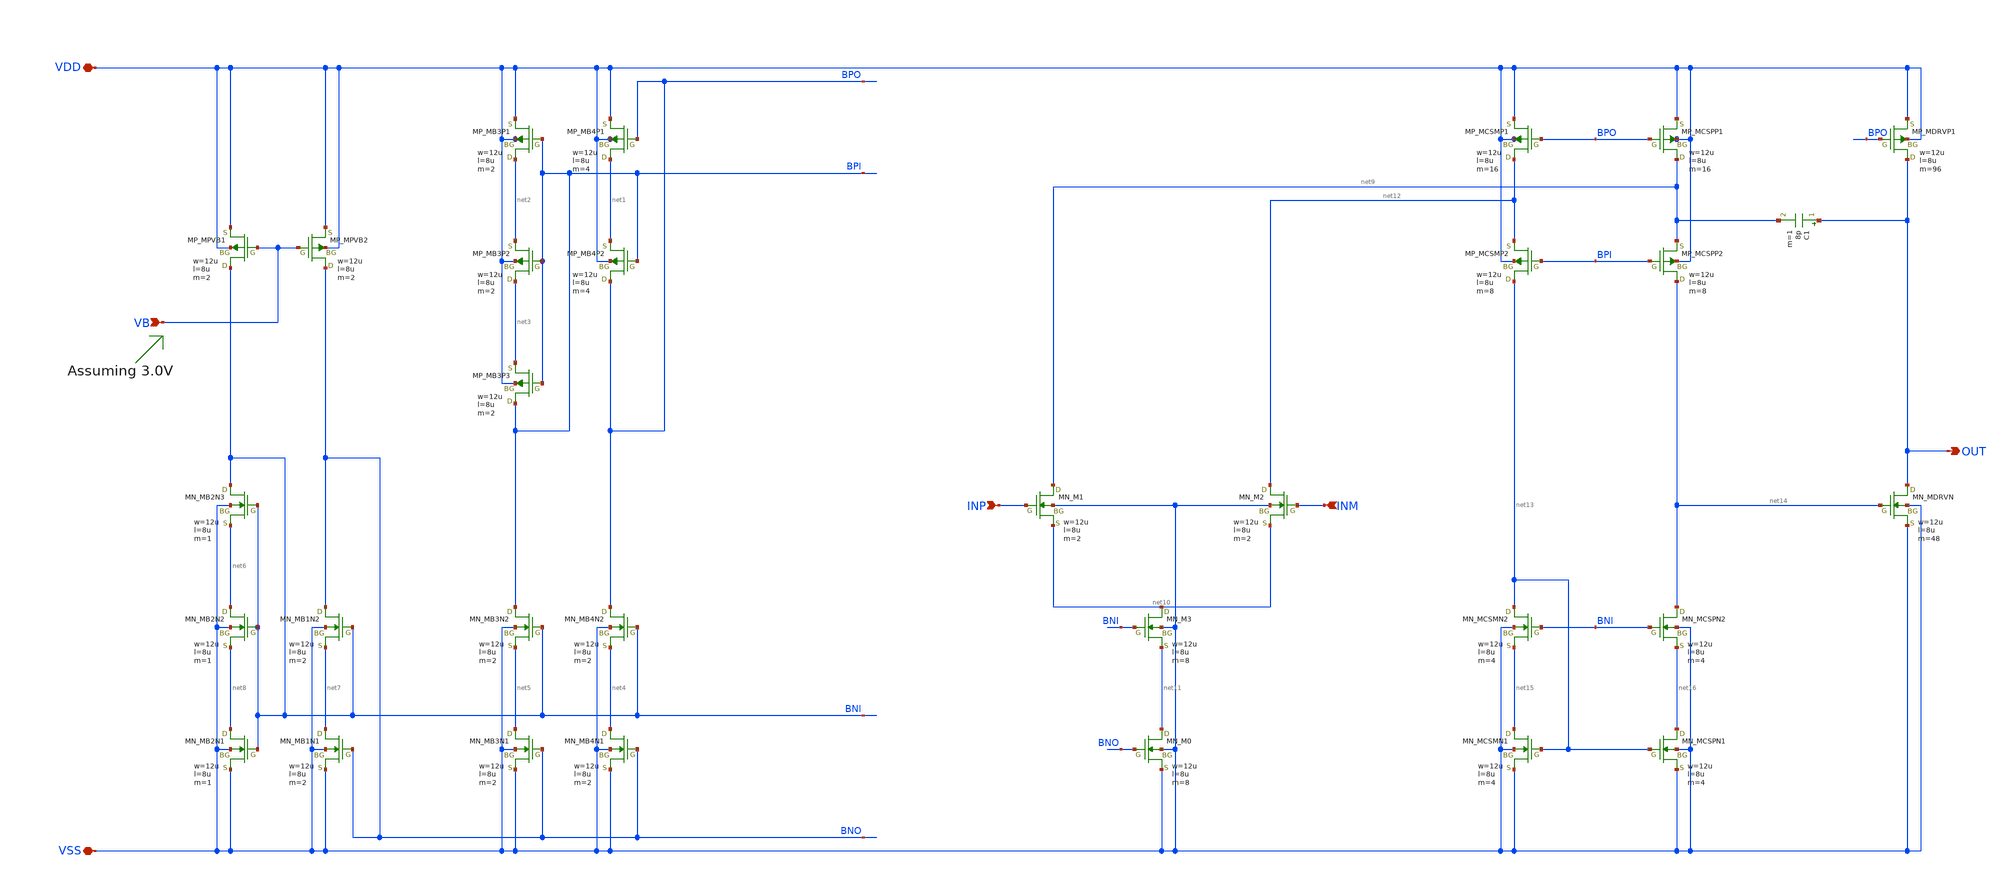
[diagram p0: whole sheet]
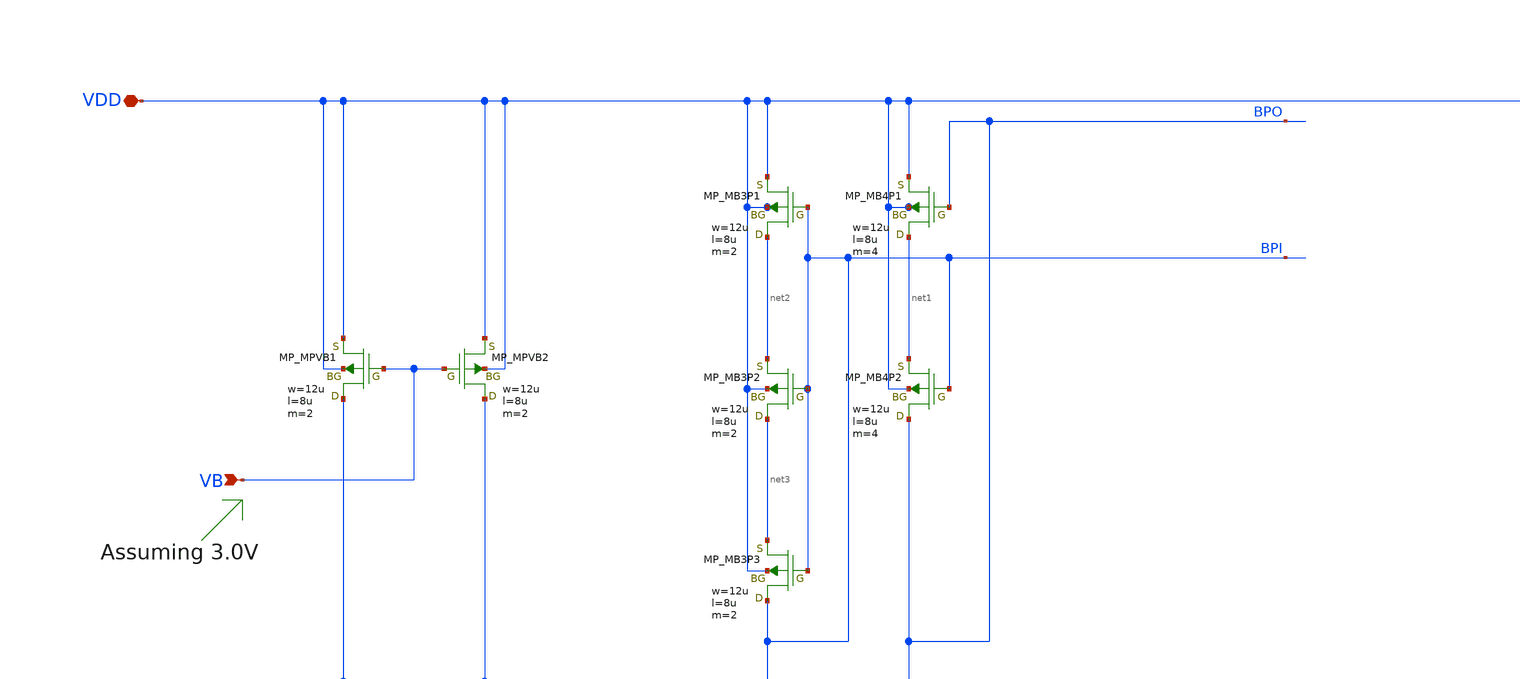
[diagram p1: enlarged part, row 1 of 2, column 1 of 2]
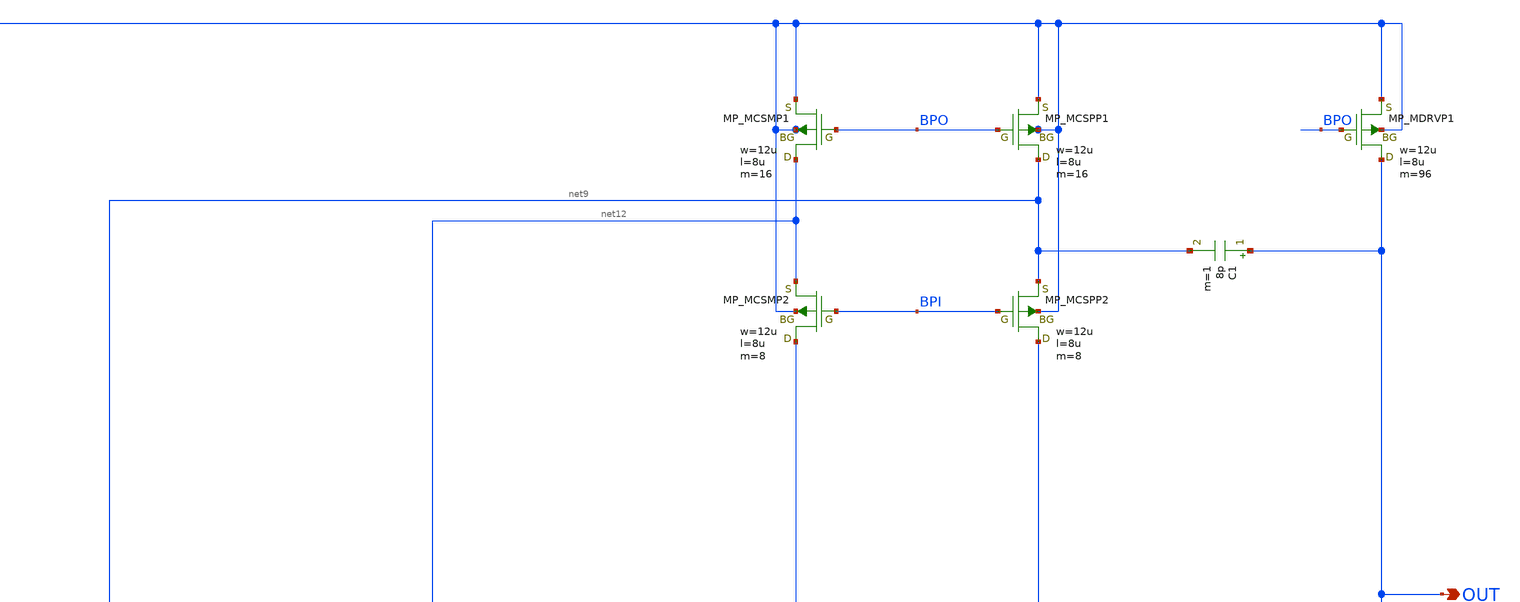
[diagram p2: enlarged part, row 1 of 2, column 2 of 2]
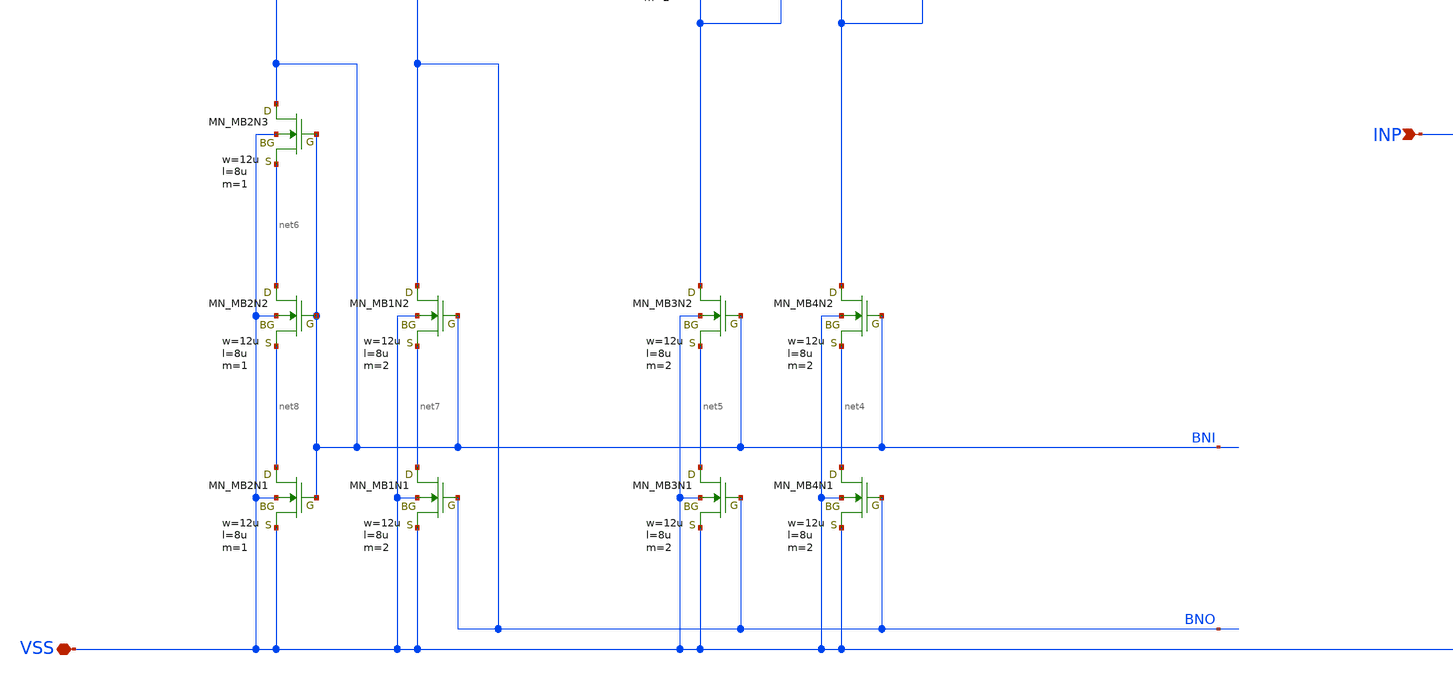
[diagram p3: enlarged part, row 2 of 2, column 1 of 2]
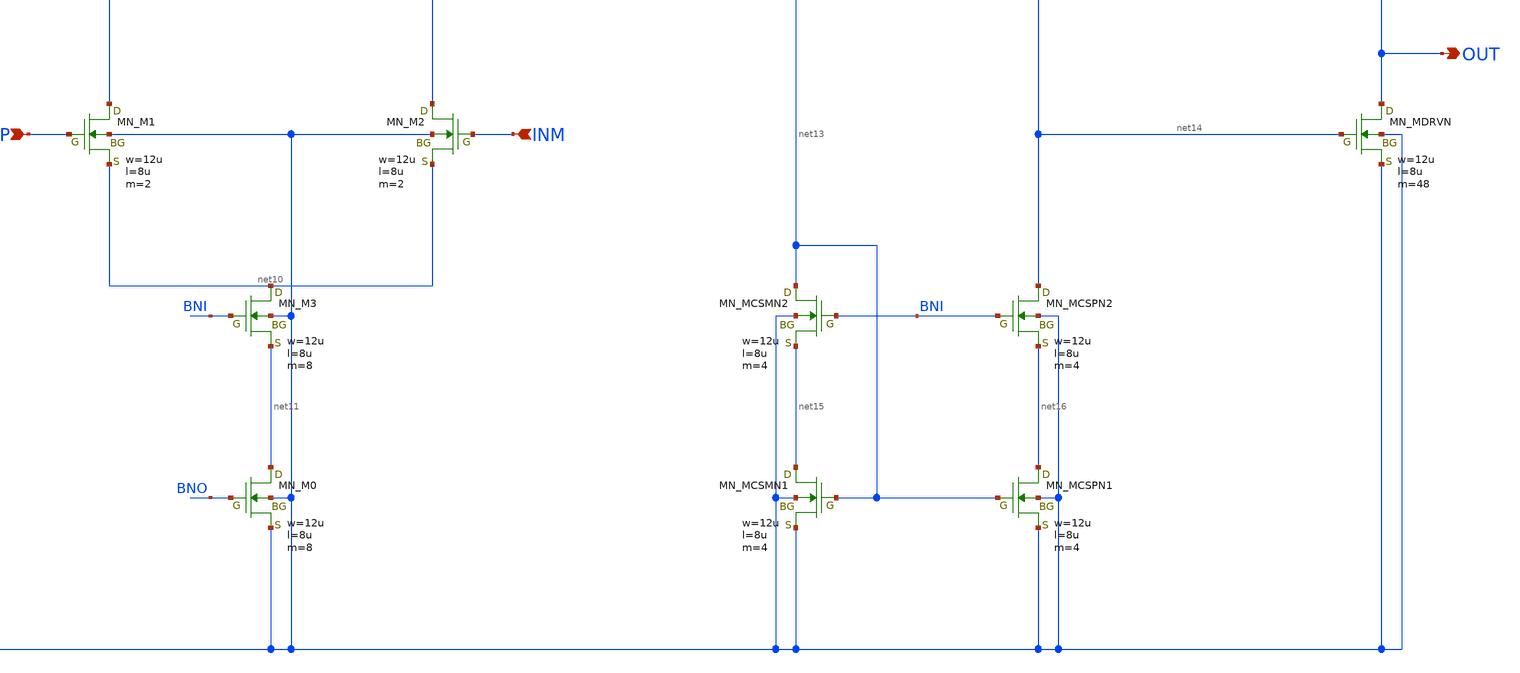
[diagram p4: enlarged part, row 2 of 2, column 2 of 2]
** sch_path: OpenSUSI-TR10/opamp_r2r/folded_sf.sch
**.subckt folded_sf VDD VSS INP INM VB OUT
*.iopin VDD
*.iopin VSS
*.ipin INP
*.ipin INM
*.ipin VB
*.opin OUT
XMB4P1 net1 BPO VDD VDD PMOS w=12u l=8u as=0 ad=0 ps=0 pd=0 nrd=0 nrs=0 m=4
XMB4P2 BPO BPI net1 VDD PMOS w=12u l=8u as=0 ad=0 ps=0 pd=0 nrd=0 nrs=0 m=4
XMB3P1 net2 BPI VDD VDD PMOS w=12u l=8u as=0 ad=0 ps=0 pd=0 nrd=0 nrs=0 m=2
XMB3P2 net3 BPI net2 VDD PMOS w=12u l=8u as=0 ad=0 ps=0 pd=0 nrd=0 nrs=0 m=2
XMB3P3 BPI BPI net3 VDD PMOS w=12u l=8u as=0 ad=0 ps=0 pd=0 nrd=0 nrs=0 m=2
XMB4N2 BPO BNI net4 VSS NMOS w=12u l=8u as=0 ad=0 ps=0 pd=0 nrd=0 nrs=0 m=2
XMB3N2 BPI BNI net5 VSS NMOS w=12u l=8u as=0 ad=0 ps=0 pd=0 nrd=0 nrs=0 m=2
XMB4N1 net4 BNO VSS VSS NMOS w=12u l=8u as=0 ad=0 ps=0 pd=0 nrd=0 nrs=0 m=2
XMB3N1 net5 BNO VSS VSS NMOS w=12u l=8u as=0 ad=0 ps=0 pd=0 nrd=0 nrs=0 m=2
XMB1N2 BNO BNI net7 VSS NMOS w=12u l=8u as=0 ad=0 ps=0 pd=0 nrd=0 nrs=0 m=2
XMB2N2 net6 BNI net8 VSS NMOS w=12u l=8u as=0 ad=0 ps=0 pd=0 nrd=0 nrs=0 m=1
XMB1N1 net7 BNO VSS VSS NMOS w=12u l=8u as=0 ad=0 ps=0 pd=0 nrd=0 nrs=0 m=2
XMB2N1 net8 BNI VSS VSS NMOS w=12u l=8u as=0 ad=0 ps=0 pd=0 nrd=0 nrs=0 m=1
XMB2N3 BNI BNI net6 VSS NMOS w=12u l=8u as=0 ad=0 ps=0 pd=0 nrd=0 nrs=0 m=1
XM3 net10 BNI net11 VSS NMOS w=12u l=8u as=0 ad=0 ps=0 pd=0 nrd=0 nrs=0 m=8
XM0 net11 BNO VSS VSS NMOS w=12u l=8u as=0 ad=0 ps=0 pd=0 nrd=0 nrs=0 m=8
XM1 net9 INP net10 VSS NMOS w=12u l=8u as=0 ad=0 ps=0 pd=0 nrd=0 nrs=0 m=2
XM2 net12 INM net10 VSS NMOS w=12u l=8u as=0 ad=0 ps=0 pd=0 nrd=0 nrs=0 m=2
XMCSMP1 net12 BPO VDD VDD PMOS w=12u l=8u as=0 ad=0 ps=0 pd=0 nrd=0 nrs=0 m=16
XMCSMP2 net13 BPI net12 VDD PMOS w=12u l=8u as=0 ad=0 ps=0 pd=0 nrd=0 nrs=0 m=8
XMCSPP1 net9 BPO VDD VDD PMOS w=12u l=8u as=0 ad=0 ps=0 pd=0 nrd=0 nrs=0 m=16
XMCSPP2 net14 BPI net9 VDD PMOS w=12u l=8u as=0 ad=0 ps=0 pd=0 nrd=0 nrs=0 m=8
XMCSMN2 net13 BNI net15 VSS NMOS w=12u l=8u as=0 ad=0 ps=0 pd=0 nrd=0 nrs=0 m=4
XMCSMN1 net15 net13 VSS VSS NMOS w=12u l=8u as=0 ad=0 ps=0 pd=0 nrd=0 nrs=0 m=4
XMCSPN2 net14 BNI net16 VSS NMOS w=12u l=8u as=0 ad=0 ps=0 pd=0 nrd=0 nrs=0 m=4
XMCSPN1 net16 net13 VSS VSS NMOS w=12u l=8u as=0 ad=0 ps=0 pd=0 nrd=0 nrs=0 m=4
XMPVB1 BNI VB VDD VDD PMOS w=12u l=8u as=0 ad=0 ps=0 pd=0 nrd=0 nrs=0 m=2
XMPVB2 BNO VB VDD VDD PMOS w=12u l=8u as=0 ad=0 ps=0 pd=0 nrd=0 nrs=0 m=2
XMDRVN OUT net14 VSS VSS NMOS w=12u l=8u as=0 ad=0 ps=0 pd=0 nrd=0 nrs=0 m=48
XMDRVP1 OUT BPO VDD VDD PMOS w=12u l=8u as=0 ad=0 ps=0 pd=0 nrd=0 nrs=0 m=96
C1 OUT net9 8p m=1
**.ends
.end
